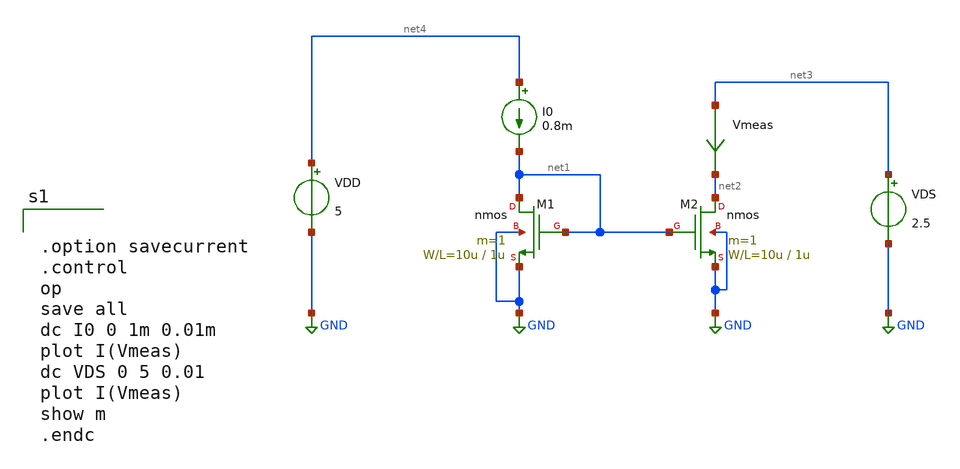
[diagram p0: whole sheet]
** sch_path: member_project/GroupWork/Team_masahiro/current_mirror.sch
**.subckt current_mirror
M1 net1 net1 GND GND nmos L=1u W=10u m=1
I0 net4 net1 0.8m
M2 net2 net1 GND GND nmos L=1u W=10u m=1
VDS net3 GND 2.5
Vmeas net3 net2 0
.save i(vmeas)
VDD net4 GND 5
**** begin user architecture code
 .include $::LIB/mos.lib
.include $::LIB/passive.lib
.include $::LIB/diode.lib


.option savecurrent
.control
op
save all
dc I0 0 1m 0.01m
plot I(Vmeas)
dc VDS 0 5 0.01
plot I(Vmeas)
show m
.endc


**** end user architecture code
**.ends
.GLOBAL GND
.end
